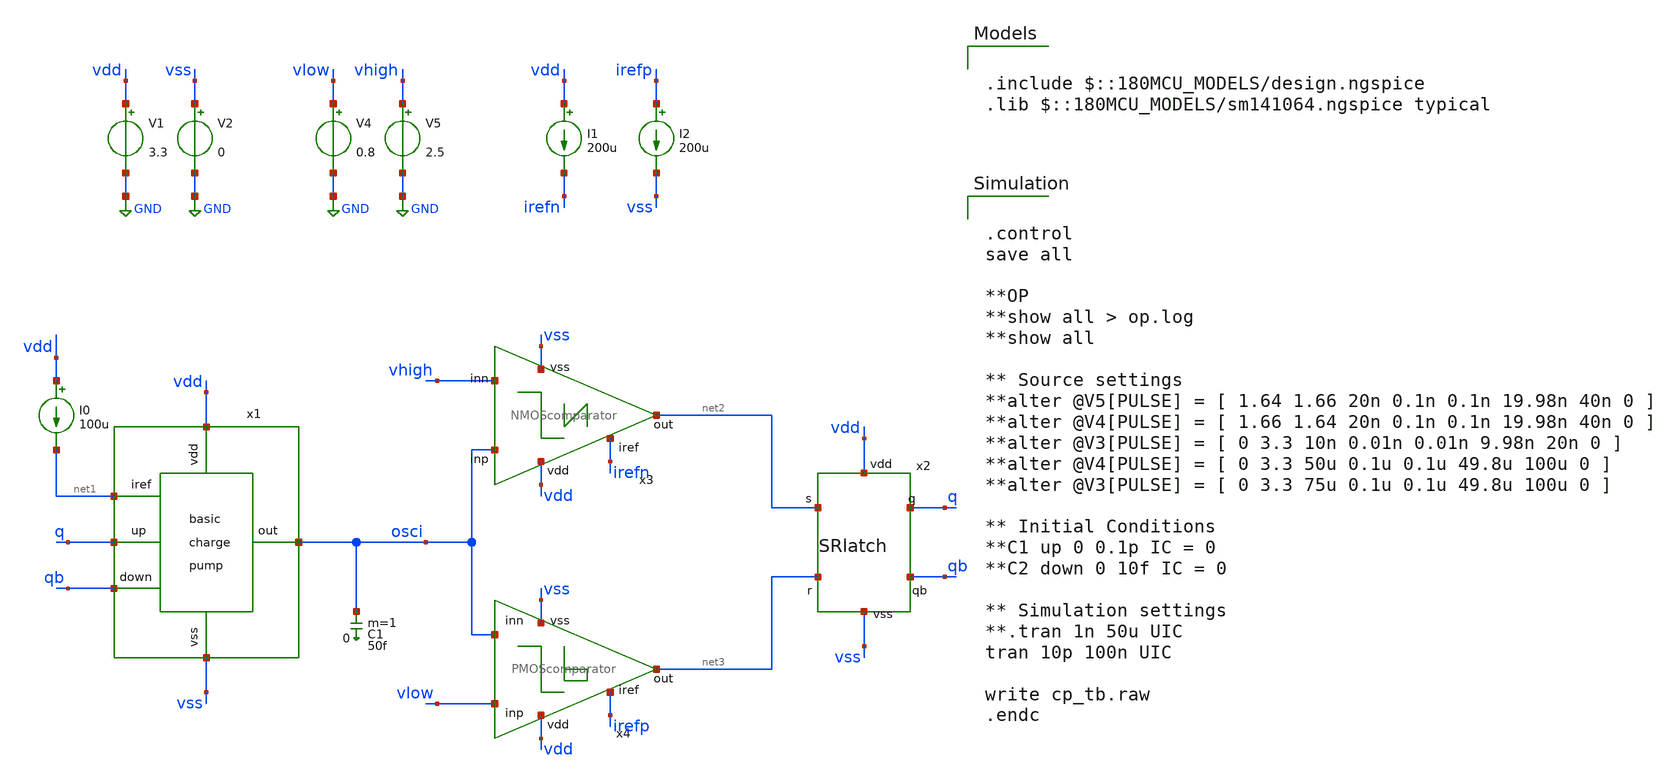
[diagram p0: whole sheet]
** sch_path: designs/libs/qw_core_analog/RVCO/relaxationVCO.sch
**.subckt relaxationVCO
x2 vdd net2 q qb net3 vss SRlatch
I0 vdd net1 100u
x1 vdd osci vss qb q net1 asc_basic_pump
V1 vdd GND 3.3
V2 vss GND 0
V4 vlow GND 0.8
V5 vhigh GND 2.5
C1 osci 0 50f m=1
x3 vdd osci net2 vhigh irefn vss NMOScomparator
x4 vdd irefp vlow net3 osci vss PMOScomparator
I1 vdd irefn 200u
I2 irefp vss 200u
**** begin user architecture code

.include $::180MCU_MODELS/design.ngspice
.lib $::180MCU_MODELS/sm141064.ngspice typical



.control
save all

**OP
**show all > op.log
**show all

** Source settings
**alter @V5[PULSE] = [ 1.64 1.66 20n 0.1n 0.1n 19.98n 40n 0 ]
**alter @V4[PULSE] = [ 1.66 1.64 20n 0.1n 0.1n 19.98n 40n 0 ]
**alter @V3[PULSE] = [ 0 3.3 10n 0.01n 0.01n 9.98n 20n 0 ]
**alter @V4[PULSE] = [ 0 3.3 50u 0.1u 0.1u 49.8u 100u 0 ]
**alter @V3[PULSE] = [ 0 3.3 75u 0.1u 0.1u 49.8u 100u 0 ]

** Initial Conditions
**C1 up 0 0.1p IC = 0
**C2 down 0 10f IC = 0

** Simulation settings
**.tran 1n 50u UIC
tran 10p 100n UIC

write cp_tb.raw
.endc


**** end user architecture code
**.ends
.GLOBAL GND
.end
